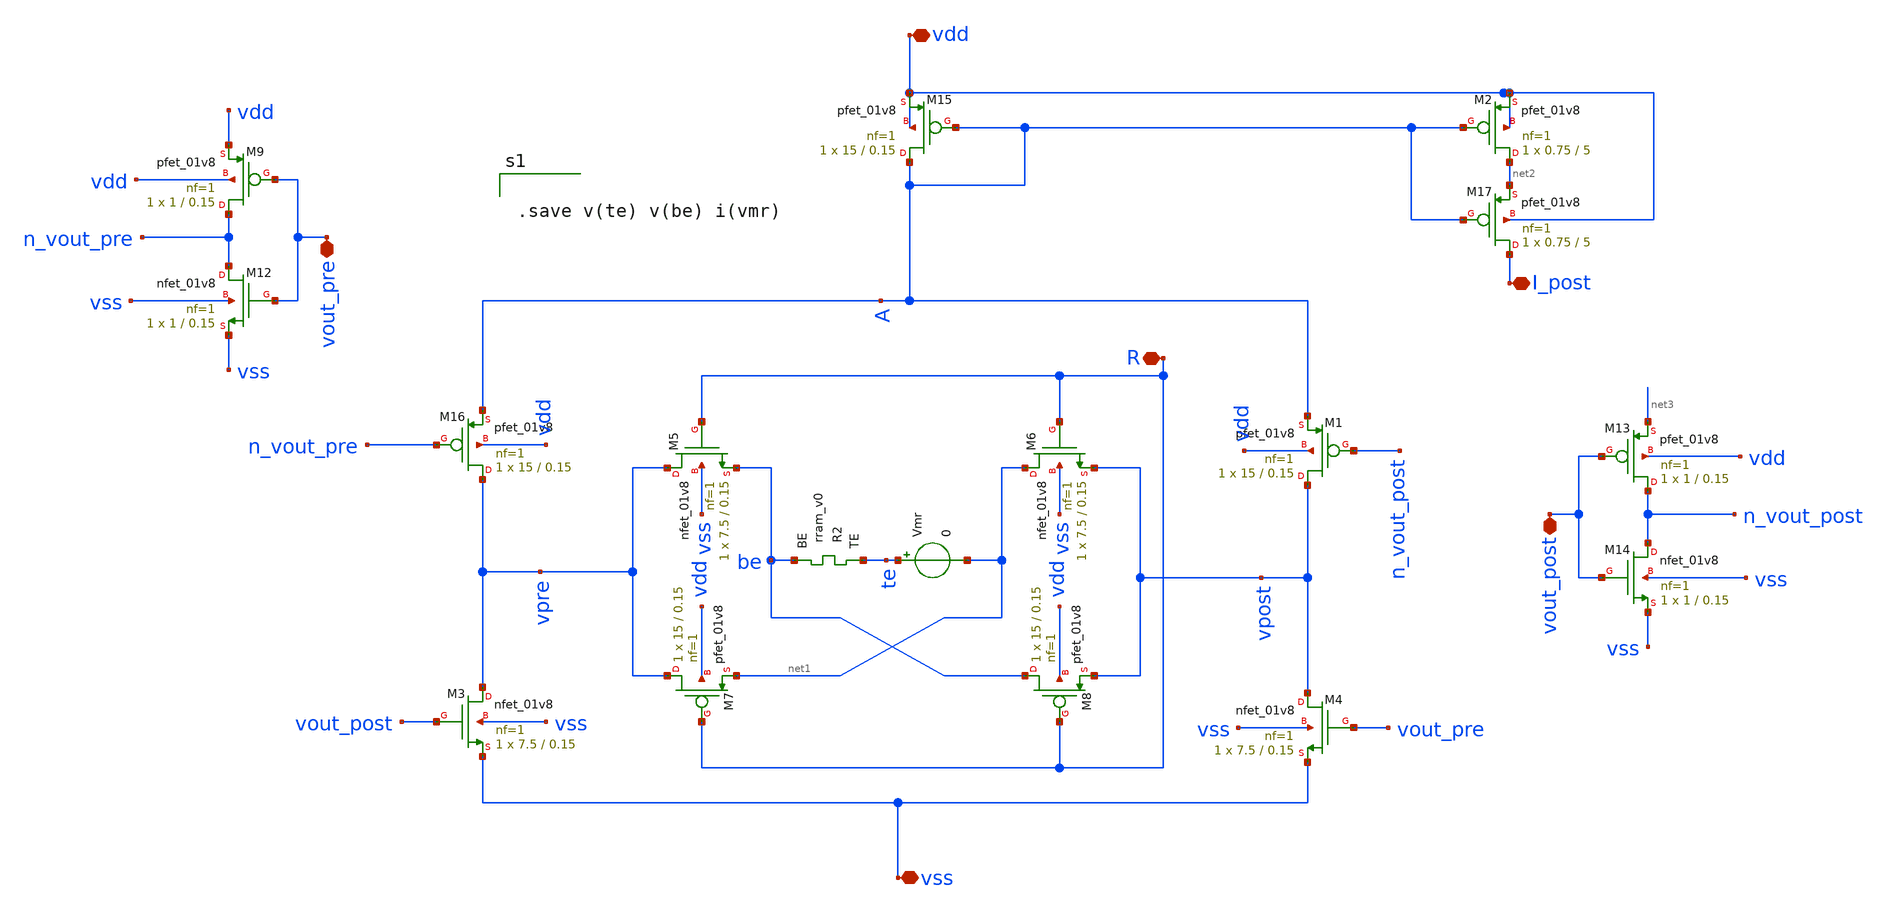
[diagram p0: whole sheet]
** sch_path: Synapse/rstdp_mirror.sch
**.subckt rstdp_mirror vdd vss R vout_post vout_pre I_post
*.iopin vdd
*.iopin vss
*.iopin R
*.iopin vout_post
*.iopin vout_pre
*.iopin I_post
XM3 vpre vout_post vss vss sky130_fd_pr__nfet_01v8 L=0.15 W=7.5 nf=1 ad='int((nf+1)/2) * W/nf * 0.29'
+ as='int((nf+2)/2) * W/nf * 0.29' pd='2*int((nf+1)/2) * (W/nf + 0.29)' ps='2*int((nf+2)/2) * (W/nf + 0.29)'
+ nrd='0.29 / W' nrs='0.29 / W' sa=0 sb=0 sd=0 mult=1 m=1
XM4 vpost vout_pre vss vss sky130_fd_pr__nfet_01v8 L=0.15 W=7.5 nf=1 ad='int((nf+1)/2) * W/nf * 0.29'
+ as='int((nf+2)/2) * W/nf * 0.29' pd='2*int((nf+1)/2) * (W/nf + 0.29)' ps='2*int((nf+2)/2) * (W/nf + 0.29)'
+ nrd='0.29 / W' nrs='0.29 / W' sa=0 sb=0 sd=0 mult=1 m=1
XR2 te be rram_v0
XM5 vpre R be vss sky130_fd_pr__nfet_01v8 L=0.15 W=7.5 nf=1 ad='int((nf+1)/2) * W/nf * 0.29' as='int((nf+2)/2) * W/nf * 0.29'
+ pd='2*int((nf+1)/2) * (W/nf + 0.29)' ps='2*int((nf+2)/2) * (W/nf + 0.29)' nrd='0.29 / W' nrs='0.29 / W'
+ sa=0 sb=0 sd=0 mult=1 m=1
XM6 net1 R vpost vss sky130_fd_pr__nfet_01v8 L=0.15 W=7.5 nf=1 ad='int((nf+1)/2) * W/nf * 0.29' as='int((nf+2)/2) * W/nf * 0.29'
+ pd='2*int((nf+1)/2) * (W/nf + 0.29)' ps='2*int((nf+2)/2) * (W/nf + 0.29)' nrd='0.29 / W' nrs='0.29 / W'
+ sa=0 sb=0 sd=0 mult=1 m=1
XM7 vpre R net1 vdd sky130_fd_pr__pfet_01v8 L=0.15 W=15 nf=1 ad='int((nf+1)/2) * W/nf * 0.29' as='int((nf+2)/2) * W/nf * 0.29'
+ pd='2*int((nf+1)/2) * (W/nf + 0.29)' ps='2*int((nf+2)/2) * (W/nf + 0.29)' nrd='0.29 / W' nrs='0.29 / W'
+ sa=0 sb=0 sd=0 mult=1 m=1
XM8 be R vpost vdd sky130_fd_pr__pfet_01v8 L=0.15 W=15 nf=1 ad='int((nf+1)/2) * W/nf * 0.29' as='int((nf+2)/2) * W/nf * 0.29'
+ pd='2*int((nf+1)/2) * (W/nf + 0.29)' ps='2*int((nf+2)/2) * (W/nf + 0.29)' nrd='0.29 / W' nrs='0.29 / W'
+ sa=0 sb=0 sd=0 mult=1 m=1
XM15 A A vdd vdd sky130_fd_pr__pfet_01v8 L=0.15 W=15 nf=1 ad='int((nf+1)/2) * W/nf * 0.29' as='int((nf+2)/2) * W/nf * 0.29'
+ pd='2*int((nf+1)/2) * (W/nf + 0.29)' ps='2*int((nf+2)/2) * (W/nf + 0.29)' nrd='0.29 / W' nrs='0.29 / W'
+ sa=0 sb=0 sd=0 mult=1 m=1
Vmr te net1 0
.save i(vmr)
XM9 n_vout_pre vout_pre vdd vdd sky130_fd_pr__pfet_01v8 L=0.15 W=1 nf=1 ad='int((nf+1)/2) * W/nf * 0.29'
+ as='int((nf+2)/2) * W/nf * 0.29' pd='2*int((nf+1)/2) * (W/nf + 0.29)' ps='2*int((nf+2)/2) * (W/nf + 0.29)'
+ nrd='0.29 / W' nrs='0.29 / W' sa=0 sb=0 sd=0 mult=1 m=1
XM12 n_vout_pre vout_pre vss vss sky130_fd_pr__nfet_01v8 L=0.15 W=1 nf=1 ad='int((nf+1)/2) * W/nf * 0.29'
+ as='int((nf+2)/2) * W/nf * 0.29' pd='2*int((nf+1)/2) * (W/nf + 0.29)' ps='2*int((nf+2)/2) * (W/nf + 0.29)'
+ nrd='0.29 / W' nrs='0.29 / W' sa=0 sb=0 sd=0 mult=1 m=1
XM13 n_vout_post vout_post net3 vdd sky130_fd_pr__pfet_01v8 L=0.15 W=1 nf=1 ad='int((nf+1)/2) * W/nf * 0.29'
+ as='int((nf+2)/2) * W/nf * 0.29' pd='2*int((nf+1)/2) * (W/nf + 0.29)' ps='2*int((nf+2)/2) * (W/nf + 0.29)'
+ nrd='0.29 / W' nrs='0.29 / W' sa=0 sb=0 sd=0 mult=1 m=1
XM14 n_vout_post vout_post vss vss sky130_fd_pr__nfet_01v8 L=0.15 W=1 nf=1 ad='int((nf+1)/2) * W/nf * 0.29'
+ as='int((nf+2)/2) * W/nf * 0.29' pd='2*int((nf+1)/2) * (W/nf + 0.29)' ps='2*int((nf+2)/2) * (W/nf + 0.29)'
+ nrd='0.29 / W' nrs='0.29 / W' sa=0 sb=0 sd=0 mult=1 m=1
XM16 vpre n_vout_pre A vdd sky130_fd_pr__pfet_01v8 L=0.15 W=15 nf=1 ad='int((nf+1)/2) * W/nf * 0.29'
+ as='int((nf+2)/2) * W/nf * 0.29' pd='2*int((nf+1)/2) * (W/nf + 0.29)' ps='2*int((nf+2)/2) * (W/nf + 0.29)'
+ nrd='0.29 / W' nrs='0.29 / W' sa=0 sb=0 sd=0 mult=1 m=1
XM1 vpost n_vout_post A vdd sky130_fd_pr__pfet_01v8 L=0.15 W=15 nf=1 ad='int((nf+1)/2) * W/nf * 0.29'
+ as='int((nf+2)/2) * W/nf * 0.29' pd='2*int((nf+1)/2) * (W/nf + 0.29)' ps='2*int((nf+2)/2) * (W/nf + 0.29)'
+ nrd='0.29 / W' nrs='0.29 / W' sa=0 sb=0 sd=0 mult=1 m=1
XM2 net2 A vdd vdd sky130_fd_pr__pfet_01v8 L=5 W=0.75 nf=1 ad='int((nf+1)/2) * W/nf * 0.29' as='int((nf+2)/2) * W/nf * 0.29'
+ pd='2*int((nf+1)/2) * (W/nf + 0.29)' ps='2*int((nf+2)/2) * (W/nf + 0.29)' nrd='0.29 / W' nrs='0.29 / W'
+ sa=0 sb=0 sd=0 mult=1 m=1
XM17 I_post A net2 vdd sky130_fd_pr__pfet_01v8 L=5 W=0.75 nf=1 ad='int((nf+1)/2) * W/nf * 0.29' as='int((nf+2)/2) * W/nf * 0.29'
+ pd='2*int((nf+1)/2) * (W/nf + 0.29)' ps='2*int((nf+2)/2) * (W/nf + 0.29)' nrd='0.29 / W' nrs='0.29 / W'
+ sa=0 sb=0 sd=0 mult=1 m=1
**** begin user architecture code


.save v(te) v(be) i(vmr)


**** end user architecture code
**.ends
.end
